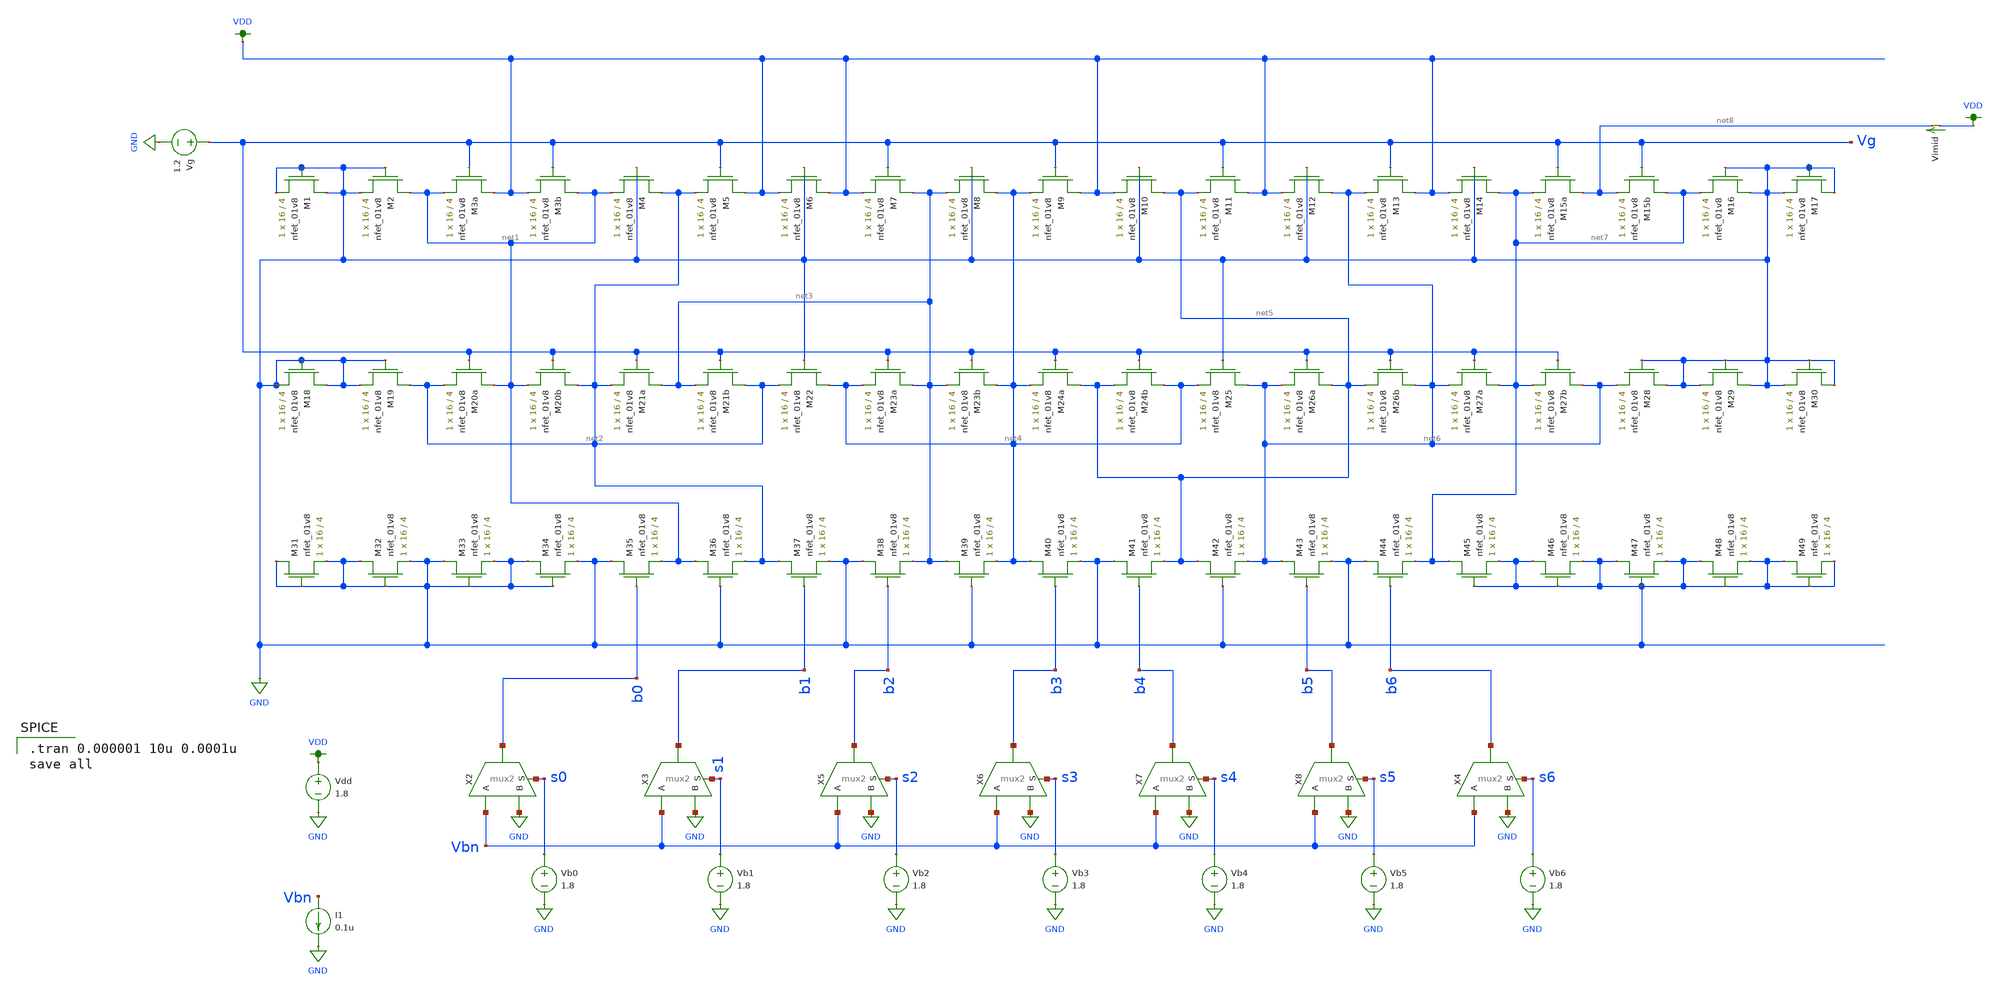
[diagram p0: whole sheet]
** sch_path: schematic/LDS/test/ladder_test.sch
**.subckt ladder_test
XM3a VDD Vg net1 GND sky130_fd_pr__nfet_01v8 L=4 W=16 nf=1 ad='int((nf+1)/2) * W/nf * 0.29' as='int((nf+2)/2) * W/nf * 0.29'
+ pd='2*int((nf+1)/2) * (W/nf + 0.29)' ps='2*int((nf+2)/2) * (W/nf + 0.29)' nrd='0.29 / W' nrs='0.29 / W'
+ sa=0 sb=0 sd=0 mult=1 m=1
XM3b net1 Vg VDD GND sky130_fd_pr__nfet_01v8 L=4 W=16 nf=1 ad='int((nf+1)/2) * W/nf * 0.29' as='int((nf+2)/2) * W/nf * 0.29'
+ pd='2*int((nf+1)/2) * (W/nf + 0.29)' ps='2*int((nf+2)/2) * (W/nf + 0.29)' nrd='0.29 / W' nrs='0.29 / W'
+ sa=0 sb=0 sd=0 mult=1 m=1
XM4 net2 GND net1 GND sky130_fd_pr__nfet_01v8 L=4 W=16 nf=1 ad='int((nf+1)/2) * W/nf * 0.29' as='int((nf+2)/2) * W/nf * 0.29'
+ pd='2*int((nf+1)/2) * (W/nf + 0.29)' ps='2*int((nf+2)/2) * (W/nf + 0.29)' nrd='0.29 / W' nrs='0.29 / W'
+ sa=0 sb=0 sd=0 mult=1 m=1
XM5 VDD Vg net2 GND sky130_fd_pr__nfet_01v8 L=4 W=16 nf=1 ad='int((nf+1)/2) * W/nf * 0.29' as='int((nf+2)/2) * W/nf * 0.29'
+ pd='2*int((nf+1)/2) * (W/nf + 0.29)' ps='2*int((nf+2)/2) * (W/nf + 0.29)' nrd='0.29 / W' nrs='0.29 / W'
+ sa=0 sb=0 sd=0 mult=1 m=1
XM6 VDD GND VDD GND sky130_fd_pr__nfet_01v8 L=4 W=16 nf=1 ad='int((nf+1)/2) * W/nf * 0.29' as='int((nf+2)/2) * W/nf * 0.29'
+ pd='2*int((nf+1)/2) * (W/nf + 0.29)' ps='2*int((nf+2)/2) * (W/nf + 0.29)' nrd='0.29 / W' nrs='0.29 / W'
+ sa=0 sb=0 sd=0 mult=1 m=1
XM7 net3 Vg VDD GND sky130_fd_pr__nfet_01v8 L=4 W=16 nf=1 ad='int((nf+1)/2) * W/nf * 0.29' as='int((nf+2)/2) * W/nf * 0.29'
+ pd='2*int((nf+1)/2) * (W/nf + 0.29)' ps='2*int((nf+2)/2) * (W/nf + 0.29)' nrd='0.29 / W' nrs='0.29 / W'
+ sa=0 sb=0 sd=0 mult=1 m=1
XM8 net4 GND net3 GND sky130_fd_pr__nfet_01v8 L=4 W=16 nf=1 ad='int((nf+1)/2) * W/nf * 0.29' as='int((nf+2)/2) * W/nf * 0.29'
+ pd='2*int((nf+1)/2) * (W/nf + 0.29)' ps='2*int((nf+2)/2) * (W/nf + 0.29)' nrd='0.29 / W' nrs='0.29 / W'
+ sa=0 sb=0 sd=0 mult=1 m=1
XM9 VDD Vg net4 GND sky130_fd_pr__nfet_01v8 L=4 W=16 nf=1 ad='int((nf+1)/2) * W/nf * 0.29' as='int((nf+2)/2) * W/nf * 0.29'
+ pd='2*int((nf+1)/2) * (W/nf + 0.29)' ps='2*int((nf+2)/2) * (W/nf + 0.29)' nrd='0.29 / W' nrs='0.29 / W'
+ sa=0 sb=0 sd=0 mult=1 m=1
XM10 net5 GND VDD GND sky130_fd_pr__nfet_01v8 L=4 W=16 nf=1 ad='int((nf+1)/2) * W/nf * 0.29' as='int((nf+2)/2) * W/nf * 0.29'
+ pd='2*int((nf+1)/2) * (W/nf + 0.29)' ps='2*int((nf+2)/2) * (W/nf + 0.29)' nrd='0.29 / W' nrs='0.29 / W'
+ sa=0 sb=0 sd=0 mult=1 m=1
XM11 VDD Vg net5 GND sky130_fd_pr__nfet_01v8 L=4 W=16 nf=1 ad='int((nf+1)/2) * W/nf * 0.29' as='int((nf+2)/2) * W/nf * 0.29'
+ pd='2*int((nf+1)/2) * (W/nf + 0.29)' ps='2*int((nf+2)/2) * (W/nf + 0.29)' nrd='0.29 / W' nrs='0.29 / W'
+ sa=0 sb=0 sd=0 mult=1 m=1
XM12 net6 GND VDD GND sky130_fd_pr__nfet_01v8 L=4 W=16 nf=1 ad='int((nf+1)/2) * W/nf * 0.29' as='int((nf+2)/2) * W/nf * 0.29'
+ pd='2*int((nf+1)/2) * (W/nf + 0.29)' ps='2*int((nf+2)/2) * (W/nf + 0.29)' nrd='0.29 / W' nrs='0.29 / W'
+ sa=0 sb=0 sd=0 mult=1 m=1
XM13 VDD Vg net6 GND sky130_fd_pr__nfet_01v8 L=4 W=16 nf=1 ad='int((nf+1)/2) * W/nf * 0.29' as='int((nf+2)/2) * W/nf * 0.29'
+ pd='2*int((nf+1)/2) * (W/nf + 0.29)' ps='2*int((nf+2)/2) * (W/nf + 0.29)' nrd='0.29 / W' nrs='0.29 / W'
+ sa=0 sb=0 sd=0 mult=1 m=1
XM14 net7 GND VDD GND sky130_fd_pr__nfet_01v8 L=4 W=16 nf=1 ad='int((nf+1)/2) * W/nf * 0.29' as='int((nf+2)/2) * W/nf * 0.29'
+ pd='2*int((nf+1)/2) * (W/nf + 0.29)' ps='2*int((nf+2)/2) * (W/nf + 0.29)' nrd='0.29 / W' nrs='0.29 / W'
+ sa=0 sb=0 sd=0 mult=1 m=1
XM15a net8 Vg net7 GND sky130_fd_pr__nfet_01v8 L=4 W=16 nf=1 ad='int((nf+1)/2) * W/nf * 0.29' as='int((nf+2)/2) * W/nf * 0.29'
+ pd='2*int((nf+1)/2) * (W/nf + 0.29)' ps='2*int((nf+2)/2) * (W/nf + 0.29)' nrd='0.29 / W' nrs='0.29 / W'
+ sa=0 sb=0 sd=0 mult=1 m=1
XM15b net7 Vg net8 GND sky130_fd_pr__nfet_01v8 L=4 W=16 nf=1 ad='int((nf+1)/2) * W/nf * 0.29' as='int((nf+2)/2) * W/nf * 0.29'
+ pd='2*int((nf+1)/2) * (W/nf + 0.29)' ps='2*int((nf+2)/2) * (W/nf + 0.29)' nrd='0.29 / W' nrs='0.29 / W'
+ sa=0 sb=0 sd=0 mult=1 m=1
XM20a net1 Vg net2 GND sky130_fd_pr__nfet_01v8 L=4 W=16 nf=1 ad='int((nf+1)/2) * W/nf * 0.29' as='int((nf+2)/2) * W/nf * 0.29'
+ pd='2*int((nf+1)/2) * (W/nf + 0.29)' ps='2*int((nf+2)/2) * (W/nf + 0.29)' nrd='0.29 / W' nrs='0.29 / W'
+ sa=0 sb=0 sd=0 mult=1 m=1
XM20b net2 Vg net1 GND sky130_fd_pr__nfet_01v8 L=4 W=16 nf=1 ad='int((nf+1)/2) * W/nf * 0.29' as='int((nf+2)/2) * W/nf * 0.29'
+ pd='2*int((nf+1)/2) * (W/nf + 0.29)' ps='2*int((nf+2)/2) * (W/nf + 0.29)' nrd='0.29 / W' nrs='0.29 / W'
+ sa=0 sb=0 sd=0 mult=1 m=1
XM21a net3 Vg net2 GND sky130_fd_pr__nfet_01v8 L=4 W=16 nf=1 ad='int((nf+1)/2) * W/nf * 0.29' as='int((nf+2)/2) * W/nf * 0.29'
+ pd='2*int((nf+1)/2) * (W/nf + 0.29)' ps='2*int((nf+2)/2) * (W/nf + 0.29)' nrd='0.29 / W' nrs='0.29 / W'
+ sa=0 sb=0 sd=0 mult=1 m=1
XM21b net2 Vg net3 GND sky130_fd_pr__nfet_01v8 L=4 W=16 nf=1 ad='int((nf+1)/2) * W/nf * 0.29' as='int((nf+2)/2) * W/nf * 0.29'
+ pd='2*int((nf+1)/2) * (W/nf + 0.29)' ps='2*int((nf+2)/2) * (W/nf + 0.29)' nrd='0.29 / W' nrs='0.29 / W'
+ sa=0 sb=0 sd=0 mult=1 m=1
XM22 net4 GND net2 GND sky130_fd_pr__nfet_01v8 L=4 W=16 nf=1 ad='int((nf+1)/2) * W/nf * 0.29' as='int((nf+2)/2) * W/nf * 0.29'
+ pd='2*int((nf+1)/2) * (W/nf + 0.29)' ps='2*int((nf+2)/2) * (W/nf + 0.29)' nrd='0.29 / W' nrs='0.29 / W'
+ sa=0 sb=0 sd=0 mult=1 m=1
XM23a net3 Vg net4 GND sky130_fd_pr__nfet_01v8 L=4 W=16 nf=1 ad='int((nf+1)/2) * W/nf * 0.29' as='int((nf+2)/2) * W/nf * 0.29'
+ pd='2*int((nf+1)/2) * (W/nf + 0.29)' ps='2*int((nf+2)/2) * (W/nf + 0.29)' nrd='0.29 / W' nrs='0.29 / W'
+ sa=0 sb=0 sd=0 mult=1 m=1
XM23b net4 Vg net3 GND sky130_fd_pr__nfet_01v8 L=4 W=16 nf=1 ad='int((nf+1)/2) * W/nf * 0.29' as='int((nf+2)/2) * W/nf * 0.29'
+ pd='2*int((nf+1)/2) * (W/nf + 0.29)' ps='2*int((nf+2)/2) * (W/nf + 0.29)' nrd='0.29 / W' nrs='0.29 / W'
+ sa=0 sb=0 sd=0 mult=1 m=1
XM24a net5 Vg net4 GND sky130_fd_pr__nfet_01v8 L=4 W=16 nf=1 ad='int((nf+1)/2) * W/nf * 0.29' as='int((nf+2)/2) * W/nf * 0.29'
+ pd='2*int((nf+1)/2) * (W/nf + 0.29)' ps='2*int((nf+2)/2) * (W/nf + 0.29)' nrd='0.29 / W' nrs='0.29 / W'
+ sa=0 sb=0 sd=0 mult=1 m=1
XM24b net4 Vg net5 GND sky130_fd_pr__nfet_01v8 L=4 W=16 nf=1 ad='int((nf+1)/2) * W/nf * 0.29' as='int((nf+2)/2) * W/nf * 0.29'
+ pd='2*int((nf+1)/2) * (W/nf + 0.29)' ps='2*int((nf+2)/2) * (W/nf + 0.29)' nrd='0.29 / W' nrs='0.29 / W'
+ sa=0 sb=0 sd=0 mult=1 m=1
XM25 net6 GND net4 GND sky130_fd_pr__nfet_01v8 L=4 W=16 nf=1 ad='int((nf+1)/2) * W/nf * 0.29' as='int((nf+2)/2) * W/nf * 0.29'
+ pd='2*int((nf+1)/2) * (W/nf + 0.29)' ps='2*int((nf+2)/2) * (W/nf + 0.29)' nrd='0.29 / W' nrs='0.29 / W'
+ sa=0 sb=0 sd=0 mult=1 m=1
XM26a net5 Vg net6 GND sky130_fd_pr__nfet_01v8 L=4 W=16 nf=1 ad='int((nf+1)/2) * W/nf * 0.29' as='int((nf+2)/2) * W/nf * 0.29'
+ pd='2*int((nf+1)/2) * (W/nf + 0.29)' ps='2*int((nf+2)/2) * (W/nf + 0.29)' nrd='0.29 / W' nrs='0.29 / W'
+ sa=0 sb=0 sd=0 mult=1 m=1
XM26b net6 Vg net5 GND sky130_fd_pr__nfet_01v8 L=4 W=16 nf=1 ad='int((nf+1)/2) * W/nf * 0.29' as='int((nf+2)/2) * W/nf * 0.29'
+ pd='2*int((nf+1)/2) * (W/nf + 0.29)' ps='2*int((nf+2)/2) * (W/nf + 0.29)' nrd='0.29 / W' nrs='0.29 / W'
+ sa=0 sb=0 sd=0 mult=1 m=1
XM27a net7 Vg net6 GND sky130_fd_pr__nfet_01v8 L=4 W=16 nf=1 ad='int((nf+1)/2) * W/nf * 0.29' as='int((nf+2)/2) * W/nf * 0.29'
+ pd='2*int((nf+1)/2) * (W/nf + 0.29)' ps='2*int((nf+2)/2) * (W/nf + 0.29)' nrd='0.29 / W' nrs='0.29 / W'
+ sa=0 sb=0 sd=0 mult=1 m=1
XM27b net6 Vg net7 GND sky130_fd_pr__nfet_01v8 L=4 W=16 nf=1 ad='int((nf+1)/2) * W/nf * 0.29' as='int((nf+2)/2) * W/nf * 0.29'
+ pd='2*int((nf+1)/2) * (W/nf + 0.29)' ps='2*int((nf+2)/2) * (W/nf + 0.29)' nrd='0.29 / W' nrs='0.29 / W'
+ sa=0 sb=0 sd=0 mult=1 m=1
XM35 GND b0 net1 GND sky130_fd_pr__nfet_01v8 L=4 W=16 nf=1 ad='int((nf+1)/2) * W/nf * 0.29' as='int((nf+2)/2) * W/nf * 0.29'
+ pd='2*int((nf+1)/2) * (W/nf + 0.29)' ps='2*int((nf+2)/2) * (W/nf + 0.29)' nrd='0.29 / W' nrs='0.29 / W'
+ sa=0 sb=0 sd=0 mult=1 m=1
XM36 net1 GND net2 GND sky130_fd_pr__nfet_01v8 L=4 W=16 nf=1 ad='int((nf+1)/2) * W/nf * 0.29' as='int((nf+2)/2) * W/nf * 0.29'
+ pd='2*int((nf+1)/2) * (W/nf + 0.29)' ps='2*int((nf+2)/2) * (W/nf + 0.29)' nrd='0.29 / W' nrs='0.29 / W'
+ sa=0 sb=0 sd=0 mult=1 m=1
XM37 net2 b1 GND GND sky130_fd_pr__nfet_01v8 L=4 W=16 nf=1 ad='int((nf+1)/2) * W/nf * 0.29' as='int((nf+2)/2) * W/nf * 0.29'
+ pd='2*int((nf+1)/2) * (W/nf + 0.29)' ps='2*int((nf+2)/2) * (W/nf + 0.29)' nrd='0.29 / W' nrs='0.29 / W'
+ sa=0 sb=0 sd=0 mult=1 m=1
XM38 GND b2 net3 GND sky130_fd_pr__nfet_01v8 L=4 W=16 nf=1 ad='int((nf+1)/2) * W/nf * 0.29' as='int((nf+2)/2) * W/nf * 0.29'
+ pd='2*int((nf+1)/2) * (W/nf + 0.29)' ps='2*int((nf+2)/2) * (W/nf + 0.29)' nrd='0.29 / W' nrs='0.29 / W'
+ sa=0 sb=0 sd=0 mult=1 m=1
XM39 net3 GND net4 GND sky130_fd_pr__nfet_01v8 L=4 W=16 nf=1 ad='int((nf+1)/2) * W/nf * 0.29' as='int((nf+2)/2) * W/nf * 0.29'
+ pd='2*int((nf+1)/2) * (W/nf + 0.29)' ps='2*int((nf+2)/2) * (W/nf + 0.29)' nrd='0.29 / W' nrs='0.29 / W'
+ sa=0 sb=0 sd=0 mult=1 m=1
XM40 net4 b3 GND GND sky130_fd_pr__nfet_01v8 L=4 W=16 nf=1 ad='int((nf+1)/2) * W/nf * 0.29' as='int((nf+2)/2) * W/nf * 0.29'
+ pd='2*int((nf+1)/2) * (W/nf + 0.29)' ps='2*int((nf+2)/2) * (W/nf + 0.29)' nrd='0.29 / W' nrs='0.29 / W'
+ sa=0 sb=0 sd=0 mult=1 m=1
XM41 GND b4 net5 GND sky130_fd_pr__nfet_01v8 L=4 W=16 nf=1 ad='int((nf+1)/2) * W/nf * 0.29' as='int((nf+2)/2) * W/nf * 0.29'
+ pd='2*int((nf+1)/2) * (W/nf + 0.29)' ps='2*int((nf+2)/2) * (W/nf + 0.29)' nrd='0.29 / W' nrs='0.29 / W'
+ sa=0 sb=0 sd=0 mult=1 m=1
XM42 net5 GND net6 GND sky130_fd_pr__nfet_01v8 L=4 W=16 nf=1 ad='int((nf+1)/2) * W/nf * 0.29' as='int((nf+2)/2) * W/nf * 0.29'
+ pd='2*int((nf+1)/2) * (W/nf + 0.29)' ps='2*int((nf+2)/2) * (W/nf + 0.29)' nrd='0.29 / W' nrs='0.29 / W'
+ sa=0 sb=0 sd=0 mult=1 m=1
XM43 net6 b5 GND GND sky130_fd_pr__nfet_01v8 L=4 W=16 nf=1 ad='int((nf+1)/2) * W/nf * 0.29' as='int((nf+2)/2) * W/nf * 0.29'
+ pd='2*int((nf+1)/2) * (W/nf + 0.29)' ps='2*int((nf+2)/2) * (W/nf + 0.29)' nrd='0.29 / W' nrs='0.29 / W'
+ sa=0 sb=0 sd=0 mult=1 m=1
XM44 GND b6 net7 GND sky130_fd_pr__nfet_01v8 L=4 W=16 nf=1 ad='int((nf+1)/2) * W/nf * 0.29' as='int((nf+2)/2) * W/nf * 0.29'
+ pd='2*int((nf+1)/2) * (W/nf + 0.29)' ps='2*int((nf+2)/2) * (W/nf + 0.29)' nrd='0.29 / W' nrs='0.29 / W'
+ sa=0 sb=0 sd=0 mult=1 m=1
XM16 GND GND net7 GND sky130_fd_pr__nfet_01v8 L=4 W=16 nf=1 ad='int((nf+1)/2) * W/nf * 0.29' as='int((nf+2)/2) * W/nf * 0.29'
+ pd='2*int((nf+1)/2) * (W/nf + 0.29)' ps='2*int((nf+2)/2) * (W/nf + 0.29)' nrd='0.29 / W' nrs='0.29 / W'
+ sa=0 sb=0 sd=0 mult=1 m=1
XM17 GND GND GND GND sky130_fd_pr__nfet_01v8 L=4 W=16 nf=1 ad='int((nf+1)/2) * W/nf * 0.29' as='int((nf+2)/2) * W/nf * 0.29'
+ pd='2*int((nf+1)/2) * (W/nf + 0.29)' ps='2*int((nf+2)/2) * (W/nf + 0.29)' nrd='0.29 / W' nrs='0.29 / W'
+ sa=0 sb=0 sd=0 mult=1 m=1
XM2 net1 GND GND GND sky130_fd_pr__nfet_01v8 L=4 W=16 nf=1 ad='int((nf+1)/2) * W/nf * 0.29' as='int((nf+2)/2) * W/nf * 0.29'
+ pd='2*int((nf+1)/2) * (W/nf + 0.29)' ps='2*int((nf+2)/2) * (W/nf + 0.29)' nrd='0.29 / W' nrs='0.29 / W'
+ sa=0 sb=0 sd=0 mult=1 m=1
XM1 GND GND GND GND sky130_fd_pr__nfet_01v8 L=4 W=16 nf=1 ad='int((nf+1)/2) * W/nf * 0.29' as='int((nf+2)/2) * W/nf * 0.29'
+ pd='2*int((nf+1)/2) * (W/nf + 0.29)' ps='2*int((nf+2)/2) * (W/nf + 0.29)' nrd='0.29 / W' nrs='0.29 / W'
+ sa=0 sb=0 sd=0 mult=1 m=1
XM19 net2 GND GND GND sky130_fd_pr__nfet_01v8 L=4 W=16 nf=1 ad='int((nf+1)/2) * W/nf * 0.29' as='int((nf+2)/2) * W/nf * 0.29'
+ pd='2*int((nf+1)/2) * (W/nf + 0.29)' ps='2*int((nf+2)/2) * (W/nf + 0.29)' nrd='0.29 / W' nrs='0.29 / W'
+ sa=0 sb=0 sd=0 mult=1 m=1
XM18 GND GND GND GND sky130_fd_pr__nfet_01v8 L=4 W=16 nf=1 ad='int((nf+1)/2) * W/nf * 0.29' as='int((nf+2)/2) * W/nf * 0.29'
+ pd='2*int((nf+1)/2) * (W/nf + 0.29)' ps='2*int((nf+2)/2) * (W/nf + 0.29)' nrd='0.29 / W' nrs='0.29 / W'
+ sa=0 sb=0 sd=0 mult=1 m=1
XM28 GND GND net6 GND sky130_fd_pr__nfet_01v8 L=4 W=16 nf=1 ad='int((nf+1)/2) * W/nf * 0.29' as='int((nf+2)/2) * W/nf * 0.29'
+ pd='2*int((nf+1)/2) * (W/nf + 0.29)' ps='2*int((nf+2)/2) * (W/nf + 0.29)' nrd='0.29 / W' nrs='0.29 / W'
+ sa=0 sb=0 sd=0 mult=1 m=1
XM29 GND GND GND GND sky130_fd_pr__nfet_01v8 L=4 W=16 nf=1 ad='int((nf+1)/2) * W/nf * 0.29' as='int((nf+2)/2) * W/nf * 0.29'
+ pd='2*int((nf+1)/2) * (W/nf + 0.29)' ps='2*int((nf+2)/2) * (W/nf + 0.29)' nrd='0.29 / W' nrs='0.29 / W'
+ sa=0 sb=0 sd=0 mult=1 m=1
XM30 GND GND GND GND sky130_fd_pr__nfet_01v8 L=4 W=16 nf=1 ad='int((nf+1)/2) * W/nf * 0.29' as='int((nf+2)/2) * W/nf * 0.29'
+ pd='2*int((nf+1)/2) * (W/nf + 0.29)' ps='2*int((nf+2)/2) * (W/nf + 0.29)' nrd='0.29 / W' nrs='0.29 / W'
+ sa=0 sb=0 sd=0 mult=1 m=1
XM45 net7 GND GND GND sky130_fd_pr__nfet_01v8 L=4 W=16 nf=1 ad='int((nf+1)/2) * W/nf * 0.29' as='int((nf+2)/2) * W/nf * 0.29'
+ pd='2*int((nf+1)/2) * (W/nf + 0.29)' ps='2*int((nf+2)/2) * (W/nf + 0.29)' nrd='0.29 / W' nrs='0.29 / W'
+ sa=0 sb=0 sd=0 mult=1 m=1
XM46 GND GND GND GND sky130_fd_pr__nfet_01v8 L=4 W=16 nf=1 ad='int((nf+1)/2) * W/nf * 0.29' as='int((nf+2)/2) * W/nf * 0.29'
+ pd='2*int((nf+1)/2) * (W/nf + 0.29)' ps='2*int((nf+2)/2) * (W/nf + 0.29)' nrd='0.29 / W' nrs='0.29 / W'
+ sa=0 sb=0 sd=0 mult=1 m=1
XM47 GND GND GND GND sky130_fd_pr__nfet_01v8 L=4 W=16 nf=1 ad='int((nf+1)/2) * W/nf * 0.29' as='int((nf+2)/2) * W/nf * 0.29'
+ pd='2*int((nf+1)/2) * (W/nf + 0.29)' ps='2*int((nf+2)/2) * (W/nf + 0.29)' nrd='0.29 / W' nrs='0.29 / W'
+ sa=0 sb=0 sd=0 mult=1 m=1
XM48 GND GND GND GND sky130_fd_pr__nfet_01v8 L=4 W=16 nf=1 ad='int((nf+1)/2) * W/nf * 0.29' as='int((nf+2)/2) * W/nf * 0.29'
+ pd='2*int((nf+1)/2) * (W/nf + 0.29)' ps='2*int((nf+2)/2) * (W/nf + 0.29)' nrd='0.29 / W' nrs='0.29 / W'
+ sa=0 sb=0 sd=0 mult=1 m=1
XM49 GND GND GND GND sky130_fd_pr__nfet_01v8 L=4 W=16 nf=1 ad='int((nf+1)/2) * W/nf * 0.29' as='int((nf+2)/2) * W/nf * 0.29'
+ pd='2*int((nf+1)/2) * (W/nf + 0.29)' ps='2*int((nf+2)/2) * (W/nf + 0.29)' nrd='0.29 / W' nrs='0.29 / W'
+ sa=0 sb=0 sd=0 mult=1 m=1
XM34 GND GND GND GND sky130_fd_pr__nfet_01v8 L=4 W=16 nf=1 ad='int((nf+1)/2) * W/nf * 0.29' as='int((nf+2)/2) * W/nf * 0.29'
+ pd='2*int((nf+1)/2) * (W/nf + 0.29)' ps='2*int((nf+2)/2) * (W/nf + 0.29)' nrd='0.29 / W' nrs='0.29 / W'
+ sa=0 sb=0 sd=0 mult=1 m=1
XM33 GND GND GND GND sky130_fd_pr__nfet_01v8 L=4 W=16 nf=1 ad='int((nf+1)/2) * W/nf * 0.29' as='int((nf+2)/2) * W/nf * 0.29'
+ pd='2*int((nf+1)/2) * (W/nf + 0.29)' ps='2*int((nf+2)/2) * (W/nf + 0.29)' nrd='0.29 / W' nrs='0.29 / W'
+ sa=0 sb=0 sd=0 mult=1 m=1
XM32 GND GND GND GND sky130_fd_pr__nfet_01v8 L=4 W=16 nf=1 ad='int((nf+1)/2) * W/nf * 0.29' as='int((nf+2)/2) * W/nf * 0.29'
+ pd='2*int((nf+1)/2) * (W/nf + 0.29)' ps='2*int((nf+2)/2) * (W/nf + 0.29)' nrd='0.29 / W' nrs='0.29 / W'
+ sa=0 sb=0 sd=0 mult=1 m=1
XM31 GND GND GND GND sky130_fd_pr__nfet_01v8 L=4 W=16 nf=1 ad='int((nf+1)/2) * W/nf * 0.29' as='int((nf+2)/2) * W/nf * 0.29'
+ pd='2*int((nf+1)/2) * (W/nf + 0.29)' ps='2*int((nf+2)/2) * (W/nf + 0.29)' nrd='0.29 / W' nrs='0.29 / W'
+ sa=0 sb=0 sd=0 mult=1 m=1
Vg Vg GND 1.2
Vdd VDD GND 1.8
I1 Vbn GND 0.1u
X2 b0 Vbn GND s0 mux2
X3 b1 Vbn GND s1 mux2
Vb0 s0 GND 1.8
Vb1 s1 GND 1.8
Vb2 s2 GND 1.8
X5 b2 Vbn GND s2 mux2
Vb3 s3 GND 1.8
X6 b3 Vbn GND s3 mux2
Vb4 s4 GND 1.8
X7 b4 Vbn GND s4 mux2
Vb5 s5 GND 1.8
X8 b5 Vbn GND s5 mux2
Vb6 s6 GND 1.8
X4 b6 Vbn GND s6 mux2
Vimid VDD net8 0
.save i(vimid)
**** begin user architecture code

.option wnflag=1
.param MC_SWITCH=0.0
.lib ~/skywater/skywater-pdk/libraries/sky130_fd_pr_ngspice/latest/models/sky130.lib.spice tt


.tran 0.000001 10u 0.0001u
save all

**** end user architecture code
**.ends
.GLOBAL VDD
.GLOBAL GND
.end
